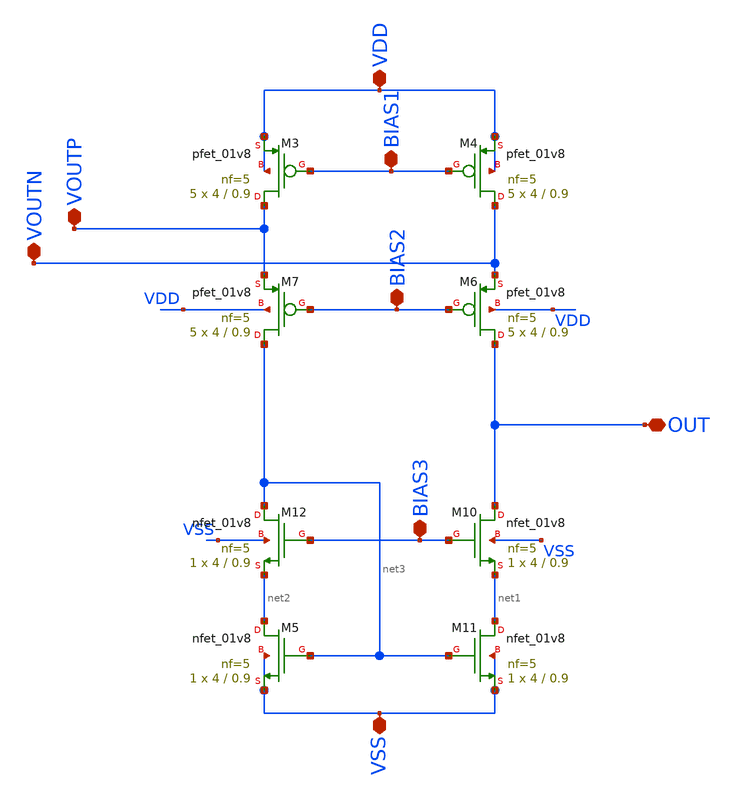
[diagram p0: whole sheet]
** sch_path: xschem/DC_DC_Converter_xschem/DC_DC_Converter/Folded_OPAMP/OPAMP3_sch.sch
**.subckt OPAMP3_sch VDD VSS VOUTP VOUTN BIAS1 BIAS2 BIAS3 OUT
*.iopin VDD
*.iopin VSS
*.iopin VOUTP
*.iopin VOUTN
*.iopin BIAS1
*.iopin BIAS2
*.iopin BIAS3
*.iopin OUT
XM3 VOUTP BIAS1 VDD VDD sky130_fd_pr__pfet_01v8 L=0.9 W=4 nf=5 ad='int((nf+1)/2) * W/nf * 0.29' as='int((nf+2)/2) * W/nf * 0.29'
+ pd='2*int((nf+1)/2) * (W/nf + 0.29)' ps='2*int((nf+2)/2) * (W/nf + 0.29)' nrd='0.29 / W' nrs='0.29 / W'
+ sa=0 sb=0 sd=0 mult=5 m=5
XM4 VOUTN BIAS1 VDD VDD sky130_fd_pr__pfet_01v8 L=0.9 W=4 nf=5 ad='int((nf+1)/2) * W/nf * 0.29' as='int((nf+2)/2) * W/nf * 0.29'
+ pd='2*int((nf+1)/2) * (W/nf + 0.29)' ps='2*int((nf+2)/2) * (W/nf + 0.29)' nrd='0.29 / W' nrs='0.29 / W'
+ sa=0 sb=0 sd=0 mult=5 m=5
XM6 OUT BIAS2 VOUTN VDD sky130_fd_pr__pfet_01v8 L=0.9 W=4 nf=5 ad='int((nf+1)/2) * W/nf * 0.29' as='int((nf+2)/2) * W/nf * 0.29'
+ pd='2*int((nf+1)/2) * (W/nf + 0.29)' ps='2*int((nf+2)/2) * (W/nf + 0.29)' nrd='0.29 / W' nrs='0.29 / W'
+ sa=0 sb=0 sd=0 mult=5 m=5
XM7 net3 BIAS2 VOUTP VDD sky130_fd_pr__pfet_01v8 L=0.9 W=4 nf=5 ad='int((nf+1)/2) * W/nf * 0.29' as='int((nf+2)/2) * W/nf * 0.29'
+ pd='2*int((nf+1)/2) * (W/nf + 0.29)' ps='2*int((nf+2)/2) * (W/nf + 0.29)' nrd='0.29 / W' nrs='0.29 / W'
+ sa=0 sb=0 sd=0 mult=5 m=5
XM10 OUT BIAS3 net1 VSS sky130_fd_pr__nfet_01v8 L=0.9 W=4 nf=5 ad='int((nf+1)/2) * W/nf * 0.29' as='int((nf+2)/2) * W/nf * 0.29'
+ pd='2*int((nf+1)/2) * (W/nf + 0.29)' ps='2*int((nf+2)/2) * (W/nf + 0.29)' nrd='0.29 / W' nrs='0.29 / W'
+ sa=0 sb=0 sd=0 mult=1 m=1
XM12 net3 BIAS3 net2 VSS sky130_fd_pr__nfet_01v8 L=0.9 W=4 nf=5 ad='int((nf+1)/2) * W/nf * 0.29' as='int((nf+2)/2) * W/nf * 0.29'
+ pd='2*int((nf+1)/2) * (W/nf + 0.29)' ps='2*int((nf+2)/2) * (W/nf + 0.29)' nrd='0.29 / W' nrs='0.29 / W'
+ sa=0 sb=0 sd=0 mult=1 m=1
XM5 net2 net3 VSS VSS sky130_fd_pr__nfet_01v8 L=0.9 W=4 nf=5 ad='int((nf+1)/2) * W/nf * 0.29' as='int((nf+2)/2) * W/nf * 0.29'
+ pd='2*int((nf+1)/2) * (W/nf + 0.29)' ps='2*int((nf+2)/2) * (W/nf + 0.29)' nrd='0.29 / W' nrs='0.29 / W'
+ sa=0 sb=0 sd=0 mult=1 m=1
XM11 net1 net3 VSS VSS sky130_fd_pr__nfet_01v8 L=0.9 W=4 nf=5 ad='int((nf+1)/2) * W/nf * 0.29' as='int((nf+2)/2) * W/nf * 0.29'
+ pd='2*int((nf+1)/2) * (W/nf + 0.29)' ps='2*int((nf+2)/2) * (W/nf + 0.29)' nrd='0.29 / W' nrs='0.29 / W'
+ sa=0 sb=0 sd=0 mult=1 m=1
**.ends
.end
